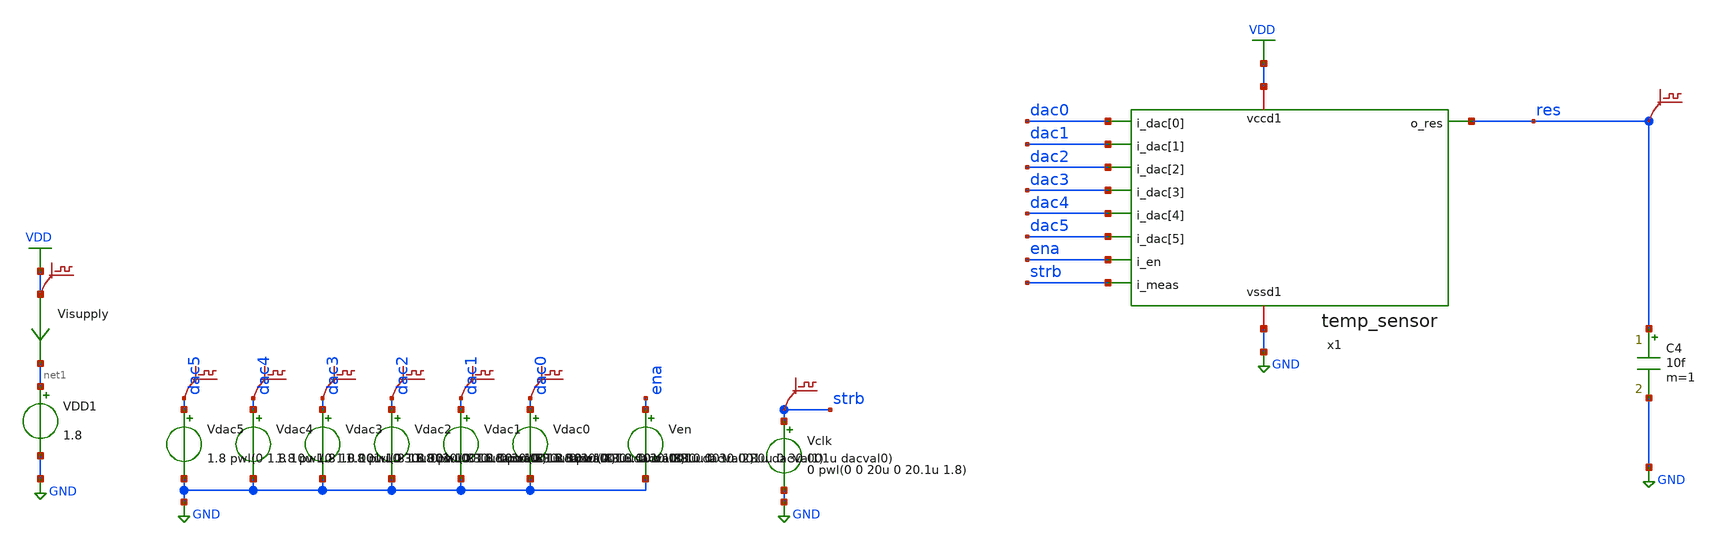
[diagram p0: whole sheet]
** sch_path: sim/tb_tempsens.sch
**.subckt tb_tempsens
VDD1 net1 GND 1.8
Vclk strb GND 0 pwl(0 0 20u 0 20.1u 1.8)
x1 dac0 dac1 dac2 dac3 dac4 dac5 ena strb res VDD GND temp_sensor
C4 res GND 10f m=1
Visupply VDD net1 0
.save i(visupply)
.save v(strb)
.save v(res)
Ven ena GND 1.8
Vdac0 dac0 GND 1.8 pwl(0 1.8 10u 1.8 10.001u 0 30u 0 30.001u dacval0)
Vdac1 dac1 GND 1.8 pwl(0 1.8 10u 1.8 10.001u 0 30u 0 30.001u dacval1)
Vdac2 dac2 GND 1.8 pwl(0 1.8 10u 1.8 10.001u 0 30u 0 30.001u dacval2)
Vdac3 dac3 GND 1.8 pwl(0 1.8 10u 1.8 10.001u 0 30u 0 30.001u dacval3)
Vdac4 dac4 GND 1.8 pwl(0 1.8 10u 1.8 10.001u 0 30u 0 30.001u dacval4)
Vdac5 dac5 GND 1.8 pwl(0 1.8 10u 1.8 10.001u 0 30u 0 30.001u dacval5)
.save v(dac5)
.save v(dac4)
.save v(dac3)
.save v(dac1)
.save v(dac0)
.save v(dac2)
.save v(vdd)
**** begin user architecture code

** opencircuitdesign pdks install
.lib sky130.lib.spice.tt.red tt





* ngspice commands
****************
.include temp_sensor.pex.spice

****************
* Misc
****************
.param dacval0=0
.param dacval1=0
.param dacval2=1.8
.param dacval3=0
.param dacval4=1.8
.param dacval5=0

.options method=gear maxord=2
.temp -30


.save x1.temp1.dac_vout_notouch_
.save x1.temp1.dcdel_capnode_notouch_


.control

tran 10u 20m

plot v(x1.temp1.dac_vout_notouch_) v(x1.temp1.dcdel_capnode_notouch_) v(res)

meas tran tmeas WHEN v(res)=0.9

let k=length(time)-1
let daccode={dac0[k]/1.8*1 + dac1[k]/1.8*2 + dac2[k]/1.8*4 + dac3[k]/1.8*8 + dac4[k]/1.8*16 + dac5[k]/1.8*32}
let vdac=v(x1.temp1.dac_vout_notouch_)[k]

*print dac tmeas > res.txt
print daccode
print vdac
print tmeas

*exit
.endc



**** end user architecture code
**.ends
.GLOBAL VDD
.GLOBAL GND
.end
